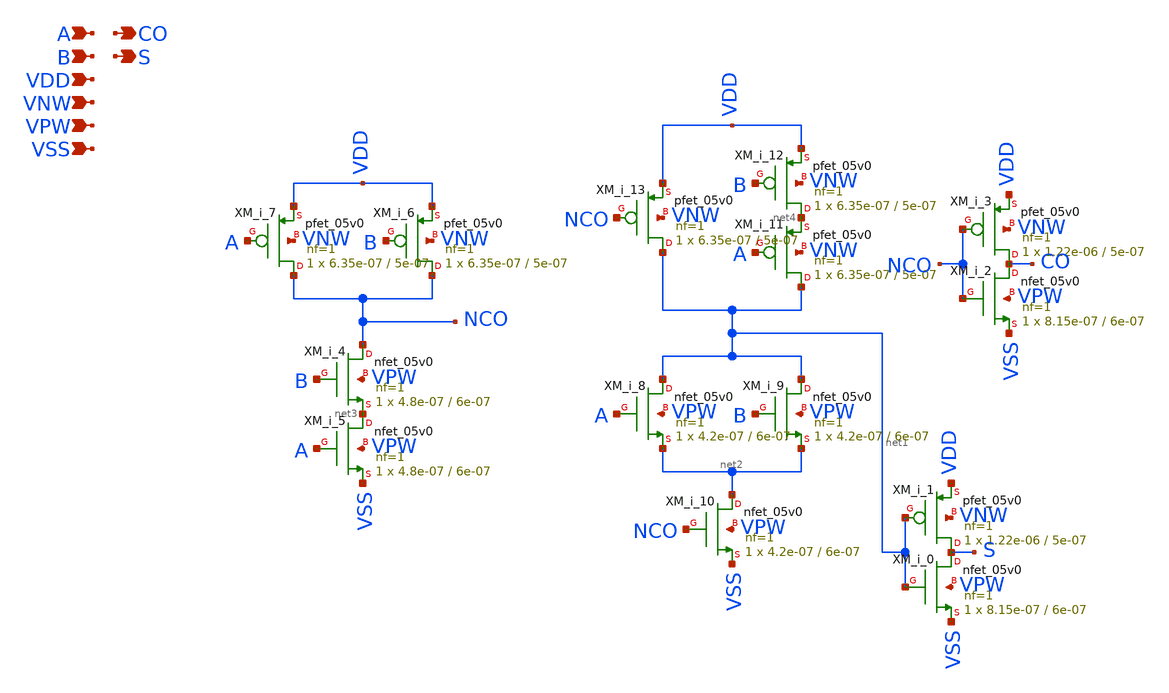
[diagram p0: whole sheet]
** sch_path: schematics/addh/gf180mcu_fd_sc_mcu7t5v0__addh_1.sch
**.subckt gf180mcu_fd_sc_mcu7t5v0__addh_1 A B CO S VDD VNW VPW VSS
*.ipin A
*.ipin B
*.opin CO
*.opin S
*.ipin VDD
*.ipin VNW
*.ipin VPW
*.ipin VSS
XM_i_3 CO NCO VDD VNW pfet_05v0 L=5e-07 W=1.22e-06 nf=1 ad='int((nf+1)/2) * W/nf * 0.18u' as='int((nf+2)/2) * W/nf * 0.18u'
+ pd='2*int((nf+1)/2) * (W/nf + 0.18u)' ps='2*int((nf+2)/2) * (W/nf + 0.18u)' nrd='0.18u / W' nrs='0.18u / W'
+ sa=0 sb=0 sd=0 m=1 par=1
XM_i_2 CO NCO VSS VPW nfet_05v0 L=6e-07 W=8.15e-07 nf=1 ad='int((nf+1)/2) * W/nf * 0.18u' as='int((nf+2)/2) * W/nf * 0.18u'
+ pd='2*int((nf+1)/2) * (W/nf + 0.18u)' ps='2*int((nf+2)/2) * (W/nf + 0.18u)' nrd='0.18u / W' nrs='0.18u / W'
+ sa=0 sb=0 sd=0 m=1
XM_i_7 NCO A VDD VNW pfet_05v0 L=5e-07 W=6.35e-07 nf=1 ad='int((nf+1)/2) * W/nf * 0.18u' as='int((nf+2)/2) * W/nf * 0.18u'
+ pd='2*int((nf+1)/2) * (W/nf + 0.18u)' ps='2*int((nf+2)/2) * (W/nf + 0.18u)' nrd='0.18u / W' nrs='0.18u / W'
+ sa=0 sb=0 sd=0 m=1 par=1
XM_i_6 NCO B VDD VNW pfet_05v0 L=5e-07 W=6.35e-07 nf=1 ad='int((nf+1)/2) * W/nf * 0.18u' as='int((nf+2)/2) * W/nf * 0.18u'
+ pd='2*int((nf+1)/2) * (W/nf + 0.18u)' ps='2*int((nf+2)/2) * (W/nf + 0.18u)' nrd='0.18u / W' nrs='0.18u / W'
+ sa=0 sb=0 sd=0 m=1 par=1
XM_i_4 NCO B net3 VPW nfet_05v0 L=6e-07 W=4.8e-07 nf=1 ad='int((nf+1)/2) * W/nf * 0.18u' as='int((nf+2)/2) * W/nf * 0.18u'
+ pd='2*int((nf+1)/2) * (W/nf + 0.18u)' ps='2*int((nf+2)/2) * (W/nf + 0.18u)' nrd='0.18u / W' nrs='0.18u / W'
+ sa=0 sb=0 sd=0 m=1
XM_i_5 net3 A VSS VPW nfet_05v0 L=6e-07 W=4.8e-07 nf=1 ad='int((nf+1)/2) * W/nf * 0.18u' as='int((nf+2)/2) * W/nf * 0.18u'
+ pd='2*int((nf+1)/2) * (W/nf + 0.18u)' ps='2*int((nf+2)/2) * (W/nf + 0.18u)' nrd='0.18u / W' nrs='0.18u / W'
+ sa=0 sb=0 sd=0 m=1
XM_i_13 net1 NCO VDD VNW pfet_05v0 L=5e-07 W=6.35e-07 nf=1 ad='int((nf+1)/2) * W/nf * 0.18u' as='int((nf+2)/2) * W/nf * 0.18u'
+ pd='2*int((nf+1)/2) * (W/nf + 0.18u)' ps='2*int((nf+2)/2) * (W/nf + 0.18u)' nrd='0.18u / W' nrs='0.18u / W'
+ sa=0 sb=0 sd=0 m=1 par=1
XM_i_12 net4 B VDD VNW pfet_05v0 L=5e-07 W=6.35e-07 nf=1 ad='int((nf+1)/2) * W/nf * 0.18u' as='int((nf+2)/2) * W/nf * 0.18u'
+ pd='2*int((nf+1)/2) * (W/nf + 0.18u)' ps='2*int((nf+2)/2) * (W/nf + 0.18u)' nrd='0.18u / W' nrs='0.18u / W'
+ sa=0 sb=0 sd=0 m=1 par=1
XM_i_11 net1 A net4 VNW pfet_05v0 L=5e-07 W=6.35e-07 nf=1 ad='int((nf+1)/2) * W/nf * 0.18u' as='int((nf+2)/2) * W/nf * 0.18u'
+ pd='2*int((nf+1)/2) * (W/nf + 0.18u)' ps='2*int((nf+2)/2) * (W/nf + 0.18u)' nrd='0.18u / W' nrs='0.18u / W'
+ sa=0 sb=0 sd=0 m=1 par=1
XM_i_8 net1 A net2 VPW nfet_05v0 L=6e-07 W=4.2e-07 nf=1 ad='int((nf+1)/2) * W/nf * 0.18u' as='int((nf+2)/2) * W/nf * 0.18u'
+ pd='2*int((nf+1)/2) * (W/nf + 0.18u)' ps='2*int((nf+2)/2) * (W/nf + 0.18u)' nrd='0.18u / W' nrs='0.18u / W'
+ sa=0 sb=0 sd=0 m=1
XM_i_9 net1 B net2 VPW nfet_05v0 L=6e-07 W=4.2e-07 nf=1 ad='int((nf+1)/2) * W/nf * 0.18u' as='int((nf+2)/2) * W/nf * 0.18u'
+ pd='2*int((nf+1)/2) * (W/nf + 0.18u)' ps='2*int((nf+2)/2) * (W/nf + 0.18u)' nrd='0.18u / W' nrs='0.18u / W'
+ sa=0 sb=0 sd=0 m=1
XM_i_10 net2 NCO VSS VPW nfet_05v0 L=6e-07 W=4.2e-07 nf=1 ad='int((nf+1)/2) * W/nf * 0.18u' as='int((nf+2)/2) * W/nf * 0.18u'
+ pd='2*int((nf+1)/2) * (W/nf + 0.18u)' ps='2*int((nf+2)/2) * (W/nf + 0.18u)' nrd='0.18u / W' nrs='0.18u / W'
+ sa=0 sb=0 sd=0 m=1
XM_i_1 S net1 VDD VNW pfet_05v0 L=5e-07 W=1.22e-06 nf=1 ad='int((nf+1)/2) * W/nf * 0.18u' as='int((nf+2)/2) * W/nf * 0.18u'
+ pd='2*int((nf+1)/2) * (W/nf + 0.18u)' ps='2*int((nf+2)/2) * (W/nf + 0.18u)' nrd='0.18u / W' nrs='0.18u / W'
+ sa=0 sb=0 sd=0 m=1 par=1
XM_i_0 S net1 VSS VPW nfet_05v0 L=6e-07 W=8.15e-07 nf=1 ad='int((nf+1)/2) * W/nf * 0.18u' as='int((nf+2)/2) * W/nf * 0.18u'
+ pd='2*int((nf+1)/2) * (W/nf + 0.18u)' ps='2*int((nf+2)/2) * (W/nf + 0.18u)' nrd='0.18u / W' nrs='0.18u / W'
+ sa=0 sb=0 sd=0 m=1
**.ends
.end
